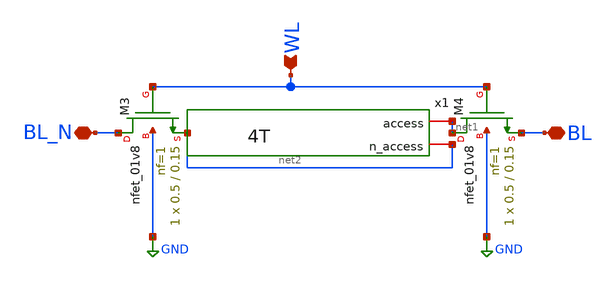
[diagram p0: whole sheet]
** sch_path: analog/schematics/Access_4T.sch
**.subckt Access_4T BL_N BL WL
*.iopin BL_N
*.iopin BL
*.ipin WL
XM3 BL_N WL net2 GND sky130_fd_pr__nfet_01v8 L=0.15 W=0.5 nf=1 ad='int((nf+1)/2) * W/nf * 0.29' as='int((nf+2)/2) * W/nf * 0.29'
+ pd='2*int((nf+1)/2) * (W/nf + 0.29)' ps='2*int((nf+2)/2) * (W/nf + 0.29)' nrd='0.29 / W' nrs='0.29 / W'
+ sa=0 sb=0 sd=0 mult=1 m=1
XM4 net1 WL BL GND sky130_fd_pr__nfet_01v8 L=0.15 W=0.5 nf=1 ad='int((nf+1)/2) * W/nf * 0.29' as='int((nf+2)/2) * W/nf * 0.29'
+ pd='2*int((nf+1)/2) * (W/nf + 0.29)' ps='2*int((nf+2)/2) * (W/nf + 0.29)' nrd='0.29 / W' nrs='0.29 / W'
+ sa=0 sb=0 sd=0 mult=1 m=1
x1 net1 net2 4T
**.ends
.GLOBAL GND
.end
